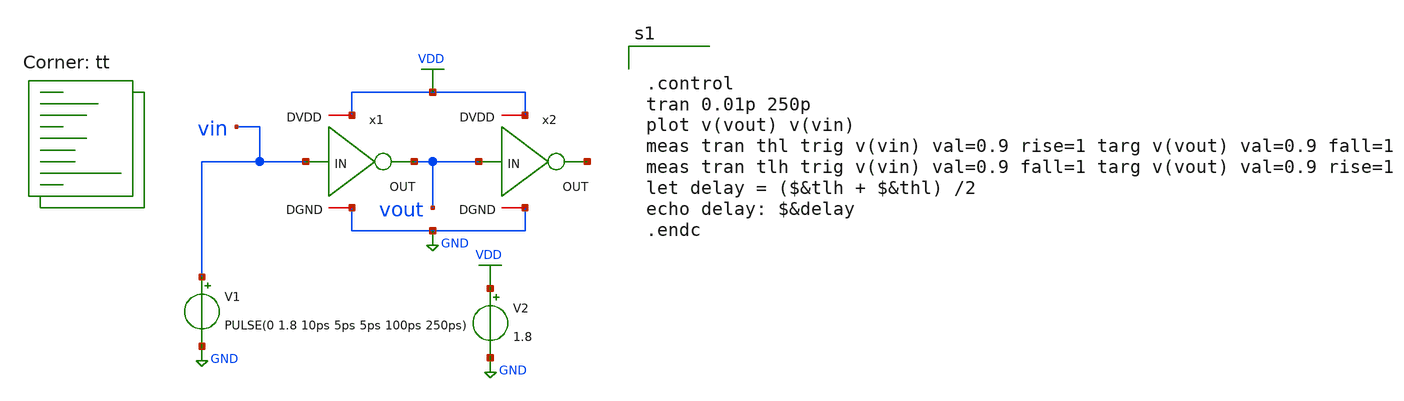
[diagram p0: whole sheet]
** sch_path: tut5/inv/sim/post-layout-again/delay.sch
**.subckt delay
x1 VDD vout vin GND inv
x2 VDD net1 vout GND inv
V1 vin GND PULSE(0 1.8 10ps 5ps 5ps 100ps 250ps)
V2 VDD GND 1.8
**** begin user architecture code
.lib $::SKYWATER_MODELS/sky130.lib.spice tt


.control
tran 0.01p 250p
plot v(vout) v(vin)
meas tran thl trig v(vin) val=0.9 rise=1 targ v(vout) val=0.9 fall=1
meas tran tlh trig v(vin) val=0.9 fall=1 targ v(vout) val=0.9 rise=1
let delay = ($&tlh + $&thl) /2
echo delay: $&delay
.endc


**** end user architecture code
**.ends

* expanding   symbol:  /home/ee24s053/ee5311-2025/tut5/inv/prim/inv.sym # of pins=4
** sym_path: tut5/inv/prim/inv.sym
** sch_path: tut5/inv/prim/inv.sch
.subckt inv DVDD OUT IN DGND
*.iopin DVDD
*.iopin DGND
*.opin OUT
*.ipin IN
XM1 OUT IN DVDD DVDD sky130_fd_pr__pfet_01v8 L=0.15 W=0.84 nf=1 ad='int((nf+1)/2) * W/nf * 0.29' as='int((nf+2)/2) * W/nf * 0.29'
+ pd='2*int((nf+1)/2) * (W/nf + 0.29)' ps='2*int((nf+2)/2) * (W/nf + 0.29)' nrd='0.29 / W' nrs='0.29 / W'
+ sa=0 sb=0 sd=0 mult=1 m=1
XM2 OUT IN DGND DGND sky130_fd_pr__nfet_01v8 L=0.15 W=0.42 nf=1 ad='int((nf+1)/2) * W/nf * 0.29' as='int((nf+2)/2) * W/nf * 0.29'
+ pd='2*int((nf+1)/2) * (W/nf + 0.29)' ps='2*int((nf+2)/2) * (W/nf + 0.29)' nrd='0.29 / W' nrs='0.29 / W'
+ sa=0 sb=0 sd=0 mult=1 m=1
.ends

.GLOBAL VDD
.GLOBAL GND
.end
